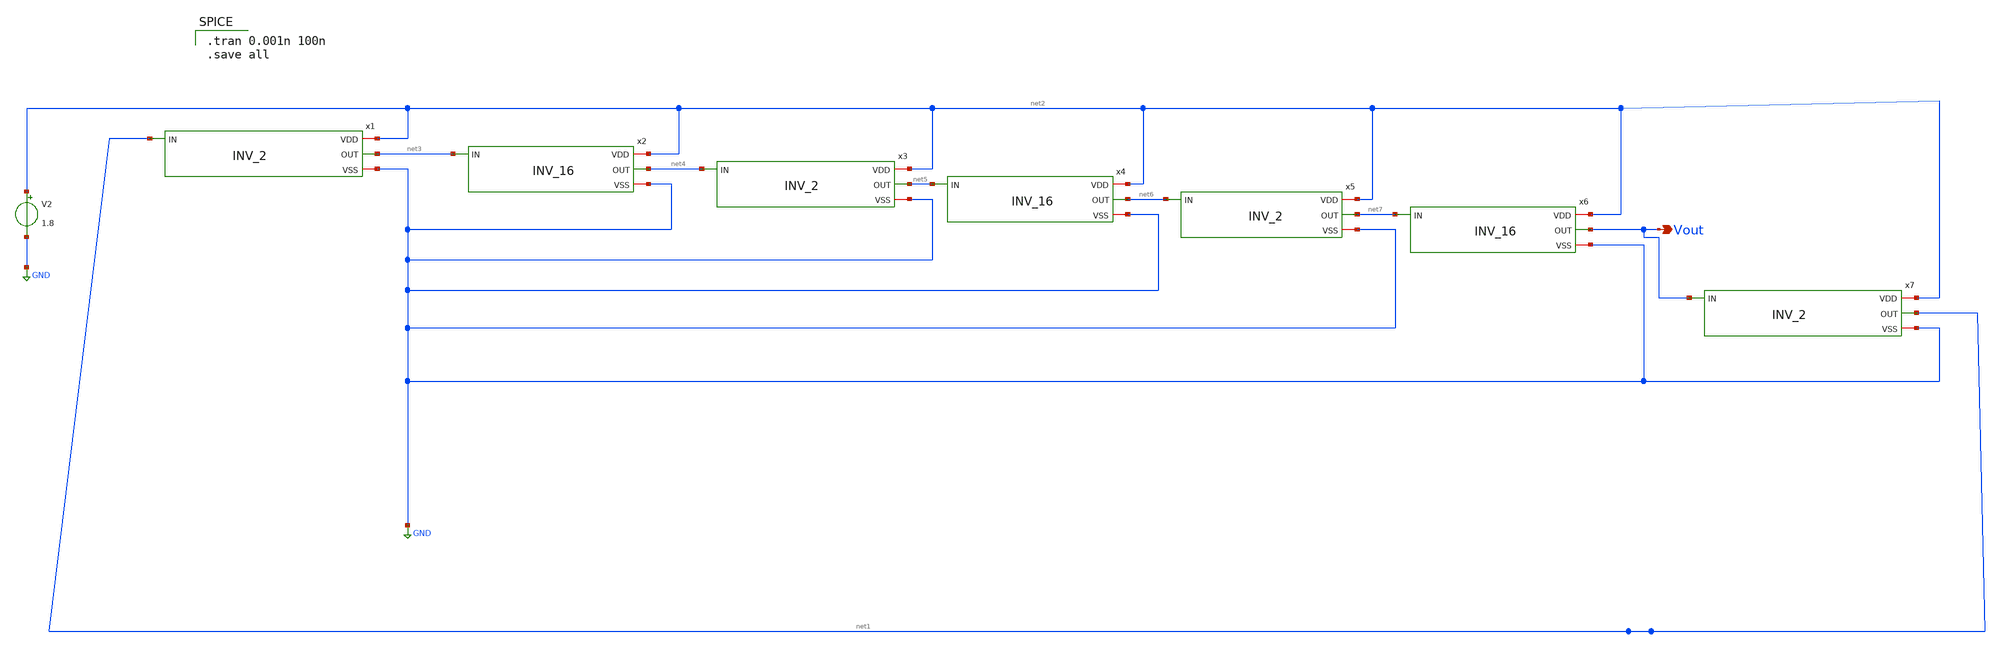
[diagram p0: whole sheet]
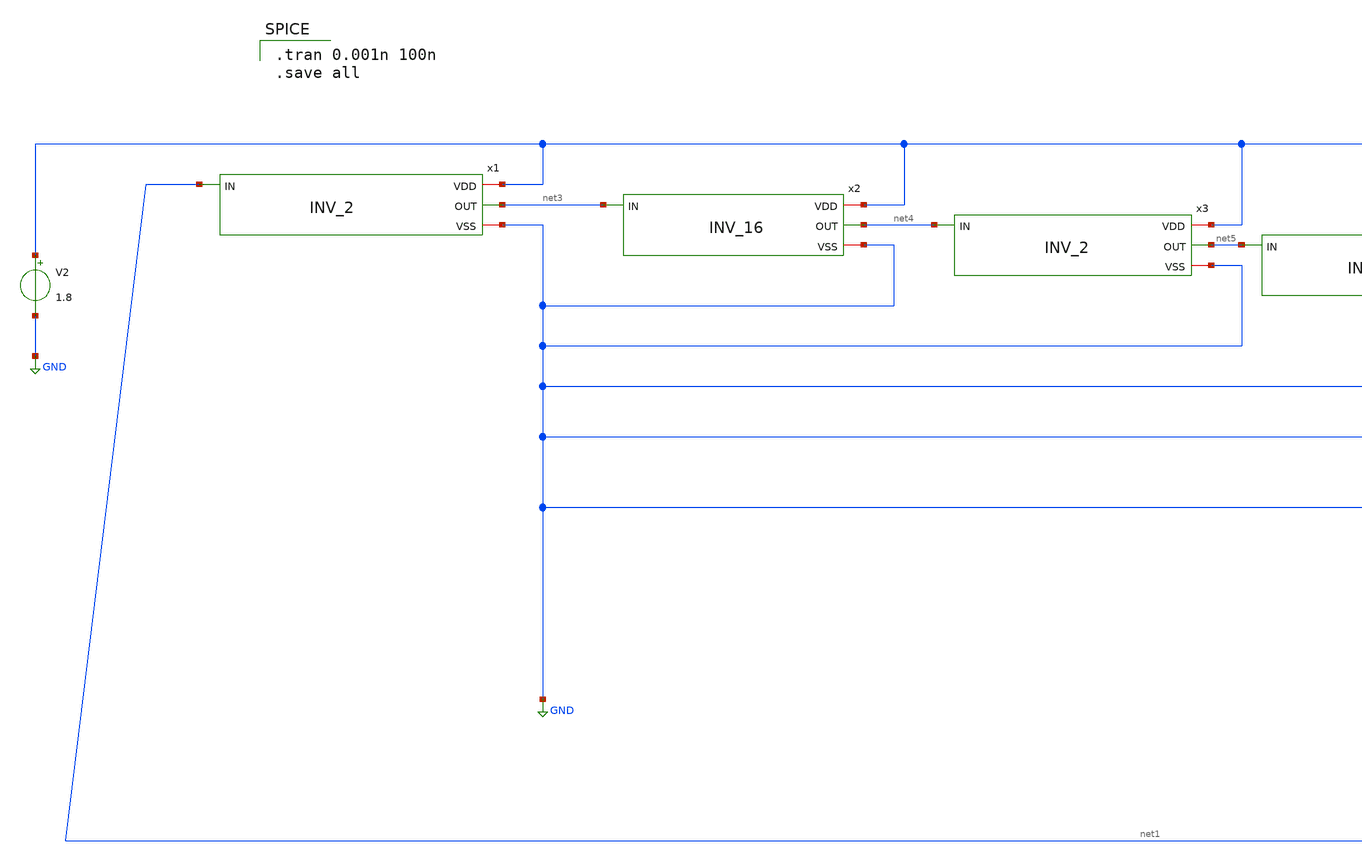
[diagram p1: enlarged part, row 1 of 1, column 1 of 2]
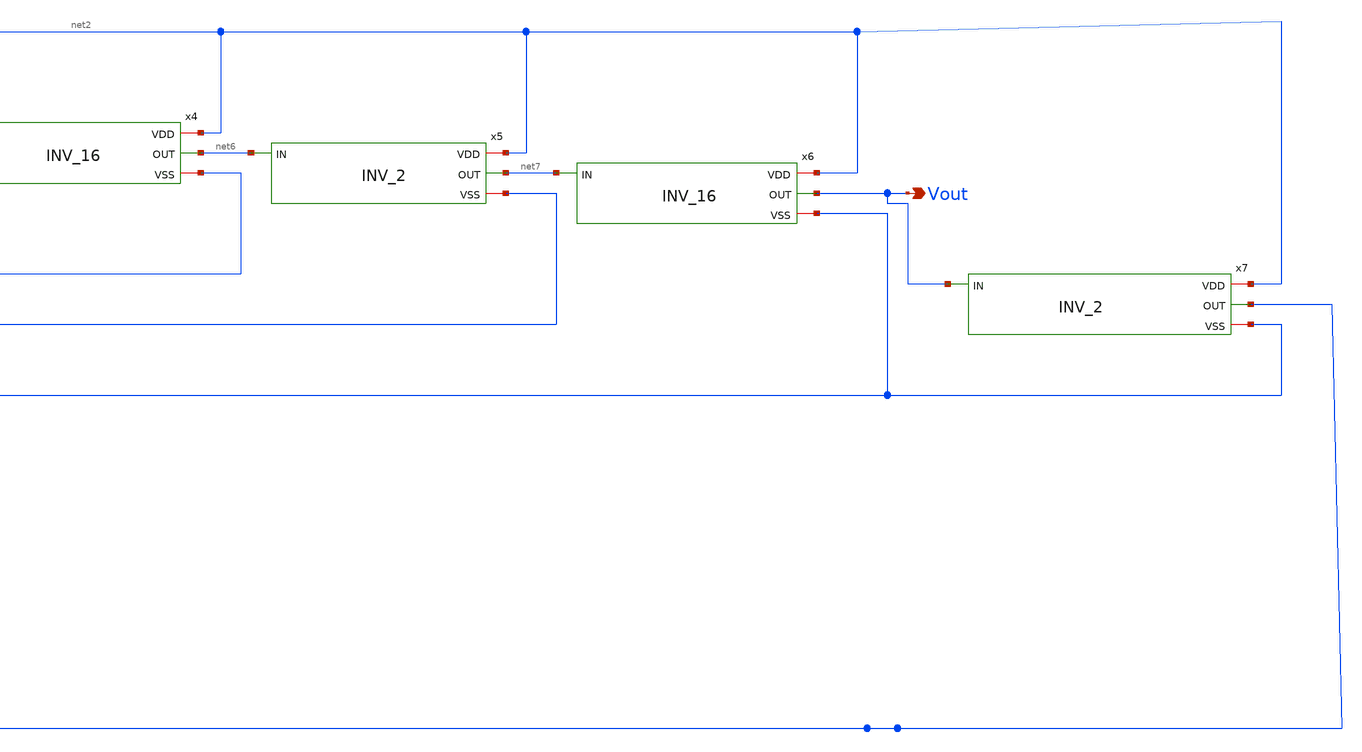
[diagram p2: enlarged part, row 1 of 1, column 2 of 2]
** sch_path: DISEÑO/ANALOGICO/V;SI/RETARDO/xschem/INV_ring_TB .sch
**.subckt INV_ring_TB  Vout
*.opin Vout
x1 net2 net1 net3 GND INV_2
V2 net2 GND 1.8
x2 net2 net3 net4 GND INV_16
x3 net2 net4 net5 GND INV_2
x4 net2 net5 net6 GND INV_16
x5 net2 net6 net7 GND INV_2
x6 net2 net7 Vout GND INV_16
x7 net2 Vout net1 GND INV_2
**** begin user architecture code

** opencircuitdesign pdks install
.lib $::SKYWATER_MODELS/sky130.lib.spice tt



.tran 0.001n 100n
.save all

**** end user architecture code
**.ends

* expanding   symbol:  INV_2.sym # of pins=4
** sym_path: DISEÑO/ANALOGICO/V;SI/RETARDO/xschem/INV_2.sym
** sch_path: DISEÑO/ANALOGICO/V;SI/RETARDO/xschem/INV_2.sch
.subckt INV_2 VDD IN OUT VSS
*.ipin IN
*.opin OUT
*.iopin VDD
*.iopin VSS
XM1 OUT IN VDD VDD sky130_fd_pr__pfet_01v8 L=0.15 W=1 nf=1 ad='int((nf+1)/2) * W/nf * 0.29' as='int((nf+2)/2) * W/nf * 0.29'
+ pd='2*int((nf+1)/2) * (W/nf + 0.29)' ps='2*int((nf+2)/2) * (W/nf + 0.29)' nrd='0.29 / W' nrs='0.29 / W'
+ sa=0 sb=0 sd=0 mult=1 m=1
XM2 OUT IN VSS VSS sky130_fd_pr__nfet_01v8 L=0.15 W=0.65 nf=1 ad='int((nf+1)/2) * W/nf * 0.29' as='int((nf+2)/2) * W/nf * 0.29'
+ pd='2*int((nf+1)/2) * (W/nf + 0.29)' ps='2*int((nf+2)/2) * (W/nf + 0.29)' nrd='0.29 / W' nrs='0.29 / W'
+ sa=0 sb=0 sd=0 mult=1 m=1
.ends


* expanding   symbol:  INV_16.sym # of pins=4
** sym_path: DISEÑO/ANALOGICO/V;SI/RETARDO/xschem/INV_16.sym
** sch_path: DISEÑO/ANALOGICO/V;SI/RETARDO/xschem/INV_16.sch
.subckt INV_16 VDD IN OUT VSS
*.ipin IN
*.opin OUT
*.iopin VDD
*.iopin VSS
XM1 OUT IN VDD VDD sky130_fd_pr__pfet_01v8 L=0.15 W=16 nf=16 ad='int((nf+1)/2) * W/nf * 0.29' as='int((nf+2)/2) * W/nf * 0.29'
+ pd='2*int((nf+1)/2) * (W/nf + 0.29)' ps='2*int((nf+2)/2) * (W/nf + 0.29)' nrd='0.29 / W' nrs='0.29 / W'
+ sa=0 sb=0 sd=0 mult=1 m=1
XM2 OUT IN VSS VSS sky130_fd_pr__nfet_01v8 L=0.15 W=10.4 nf=2 ad='int((nf+1)/2) * W/nf * 0.29' as='int((nf+2)/2) * W/nf * 0.29'
+ pd='2*int((nf+1)/2) * (W/nf + 0.29)' ps='2*int((nf+2)/2) * (W/nf + 0.29)' nrd='0.29 / W' nrs='0.29 / W'
+ sa=0 sb=0 sd=0 mult=1 m=1
.ends

.GLOBAL GND
.end
